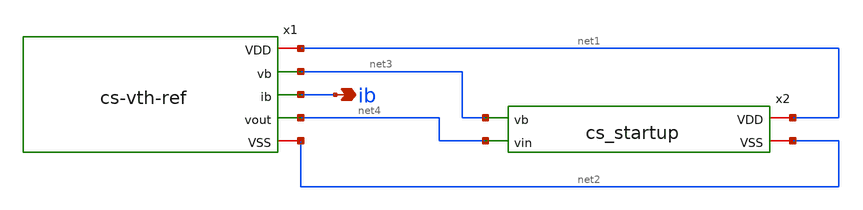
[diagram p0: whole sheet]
** sch_path: schematic/20250924_OSS_Workshop/ishikai/CS/cs_startup_usage.sch
**.subckt cs_startup_usage ib
*.opin ib
x1 net1 net3 ib net4 net2 cs-vth-ref
x2 net1 net3 net4 net2 cs_startup
**.ends

* expanding   symbol:  cs-vth-ref.sym # of pins=5
** sym_path: schematic/20250924_OSS_Workshop/ishikai/CS/cs-vth-ref.sym
** sch_path: schematic/20250924_OSS_Workshop/ishikai/CS/cs-vth-ref.sch
.subckt cs-vth-ref VDD vb ib vout VSS
*.iopin VSS
*.iopin VDD
*.opin ib
*.opin vb
*.opin vout
XM1 net1 vout VSS VSS NMOS w=50u l=1u as=0 ad=0 ps=0 pd=0 nrd=0 nrs=0 m=1
XM2 vb net1 vout VSS NMOS w=50u l=1u as=0 ad=0 ps=0 pd=0 nrd=0 nrs=0 m=1
XM3 net1 vb VDD VDD PMOS w=150u l=1u as=0 ad=0 ps=0 pd=0 nrd=0 nrs=0 m=1
XM4 vb vb VDD VDD PMOS w=150u l=1u as=0 ad=0 ps=0 pd=0 nrd=0 nrs=0 m=1
XR2 vout net2 F_RS w=4e-6 R=3000 l=100e-6 tc1=0 tc2=0
XR1 net2 net3 F_RS w=4e-6 R=3000 l=100e-6 tc1=0 tc2=0
XR3 net3 net8 F_RS w=4e-6 R=3000 l=100e-6 tc1=0 tc2=0
XR4 net8 net4 F_RS w=4e-6 R=3000 l=100e-6 tc1=0 tc2=0
XR5 net4 net5 F_RS w=4e-6 R=3000 l=100e-6 tc1=0 tc2=0
XR6 net5 net9 F_RS w=4e-6 R=3000 l=100e-6 tc1=0 tc2=0
XR7 net9 net6 F_RS w=4e-6 R=3000 l=100e-6 tc1=0 tc2=0
XR8 net6 net7 F_RS w=4e-6 R=3000 l=100e-6 tc1=0 tc2=0
XR9 net7 VSS F_RS w=4e-6 R=3000 l=100e-6 tc1=0 tc2=0
XM5 net10 vb VDD VDD PMOS w=30u l=1u as=0 ad=0 ps=0 pd=0 nrd=0 nrs=0 m=1
XM6 net10 net10 VSS VSS NMOS w=10u l=1u as=0 ad=0 ps=0 pd=0 nrd=0 nrs=0 m=1
XM7 ib net10 VSS VSS NMOS w=10u l=1u as=0 ad=0 ps=0 pd=0 nrd=0 nrs=0 m=1
.ends


* expanding   symbol:  cs_startup.sym # of pins=4
** sym_path: schematic/20250924_OSS_Workshop/ishikai/CS/cs_startup.sym
** sch_path: schematic/20250924_OSS_Workshop/ishikai/CS/cs_startup.sch
.subckt cs_startup VDD vb vin VSS
*.iopin VDD
*.iopin VSS
*.ipin vin
*.ipin vb
XM1 net1 vin VDD VDD PMOS w=3.4u l=1u as=0 ad=0 ps=0 pd=0 nrd=0 nrs=0 m=1
XM2 net1 vin VSS VSS NMOS w=1000u l=1u as=0 ad=0 ps=0 pd=0 nrd=0 nrs=0 m=1
XM3 vb net1 VSS VSS NMOS w=50u l=1u as=0 ad=0 ps=0 pd=0 nrd=0 nrs=0 m=1
.ends

.end
